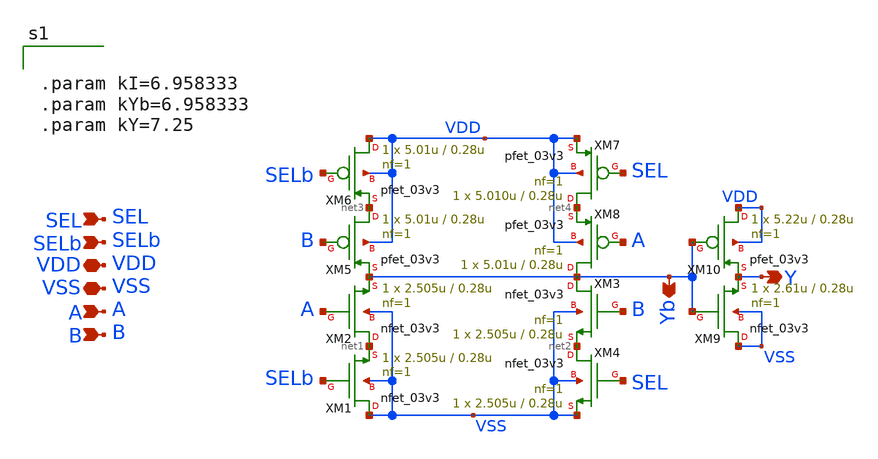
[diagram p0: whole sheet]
** sch_path: CAD5/2x1_mux_cmos.sch
**.subckt 2x1_mux_cmos A B SEL Y VDD VSS SELb Yb
*.ipin A
*.ipin B
*.ipin SEL
*.opin Y
*.iopin VDD
*.iopin VSS
*.ipin SELb
*.opin Yb
XM1 VSS SELb net1 VSS nfet_03v3 L=0.28u W=2.505u nf=1 ad='int((nf+1)/2) * W/nf * 0.18u' as='int((nf+2)/2) * W/nf * 0.18u'
+ pd='2*int((nf+1)/2) * (W/nf + 0.18u)' ps='2*int((nf+2)/2) * (W/nf + 0.18u)' nrd='0.18u / W' nrs='0.18u / W'
+ sa=0 sb=0 sd=0 m=1
XM2 net1 A Yb VSS nfet_03v3 L=0.28u W=2.505u nf=1 ad='int((nf+1)/2) * W/nf * 0.18u' as='int((nf+2)/2) * W/nf * 0.18u'
+ pd='2*int((nf+1)/2) * (W/nf + 0.18u)' ps='2*int((nf+2)/2) * (W/nf + 0.18u)' nrd='0.18u / W' nrs='0.18u / W'
+ sa=0 sb=0 sd=0 m=1
XM3 Yb B net2 VSS nfet_03v3 L=0.28u W=2.505u nf=1 ad='int((nf+1)/2) * W/nf * 0.18u' as='int((nf+2)/2) * W/nf * 0.18u'
+ pd='2*int((nf+1)/2) * (W/nf + 0.18u)' ps='2*int((nf+2)/2) * (W/nf + 0.18u)' nrd='0.18u / W' nrs='0.18u / W'
+ sa=0 sb=0 sd=0 m=1
XM4 net2 SEL VSS VSS nfet_03v3 L=0.28u W=2.505u nf=1 ad='int((nf+1)/2) * W/nf * 0.18u' as='int((nf+2)/2) * W/nf * 0.18u'
+ pd='2*int((nf+1)/2) * (W/nf + 0.18u)' ps='2*int((nf+2)/2) * (W/nf + 0.18u)' nrd='0.18u / W' nrs='0.18u / W'
+ sa=0 sb=0 sd=0 m=1
XM5 net3 B Yb VDD pfet_03v3 L=0.28u W=5.01u nf=1 ad='int((nf+1)/2) * W/nf * 0.18u' as='int((nf+2)/2) * W/nf * 0.18u'
+ pd='2*int((nf+1)/2) * (W/nf + 0.18u)' ps='2*int((nf+2)/2) * (W/nf + 0.18u)' nrd='0.18u / W' nrs='0.18u / W'
+ sa=0 sb=0 sd=0 m=1
XM6 VDD SELb net3 VDD pfet_03v3 L=0.28u W=5.01u nf=1 ad='int((nf+1)/2) * W/nf * 0.18u' as='int((nf+2)/2) * W/nf * 0.18u'
+ pd='2*int((nf+1)/2) * (W/nf + 0.18u)' ps='2*int((nf+2)/2) * (W/nf + 0.18u)' nrd='0.18u / W' nrs='0.18u / W'
+ sa=0 sb=0 sd=0 m=1
XM7 net4 SEL VDD VDD pfet_03v3 L=0.28u W=5.010u nf=1 ad='int((nf+1)/2) * W/nf * 0.18u' as='int((nf+2)/2) * W/nf * 0.18u'
+ pd='2*int((nf+1)/2) * (W/nf + 0.18u)' ps='2*int((nf+2)/2) * (W/nf + 0.18u)' nrd='0.18u / W' nrs='0.18u / W'
+ sa=0 sb=0 sd=0 m=1
XM8 Yb A net4 VDD pfet_03v3 L=0.28u W=5.01u nf=1 ad='int((nf+1)/2) * W/nf * 0.18u' as='int((nf+2)/2) * W/nf * 0.18u'
+ pd='2*int((nf+1)/2) * (W/nf + 0.18u)' ps='2*int((nf+2)/2) * (W/nf + 0.18u)' nrd='0.18u / W' nrs='0.18u / W'
+ sa=0 sb=0 sd=0 m=1
XM9 VSS Yb Y VSS nfet_03v3 L=0.28u W=2.61u nf=1 ad='int((nf+1)/2) * W/nf * 0.18u' as='int((nf+2)/2) * W/nf * 0.18u'
+ pd='2*int((nf+1)/2) * (W/nf + 0.18u)' ps='2*int((nf+2)/2) * (W/nf + 0.18u)' nrd='0.18u / W' nrs='0.18u / W'
+ sa=0 sb=0 sd=0 m=1
XM10 VDD Yb Y VDD pfet_03v3 L=0.28u W=5.22u nf=1 ad='int((nf+1)/2) * W/nf * 0.18u' as='int((nf+2)/2) * W/nf * 0.18u'
+ pd='2*int((nf+1)/2) * (W/nf + 0.18u)' ps='2*int((nf+2)/2) * (W/nf + 0.18u)' nrd='0.18u / W' nrs='0.18u / W'
+ sa=0 sb=0 sd=0 m=1
**** begin user architecture code


.param kI=6.958333
.param kYb=6.958333
.param kY=7.25


**** end user architecture code
**.ends
.end
